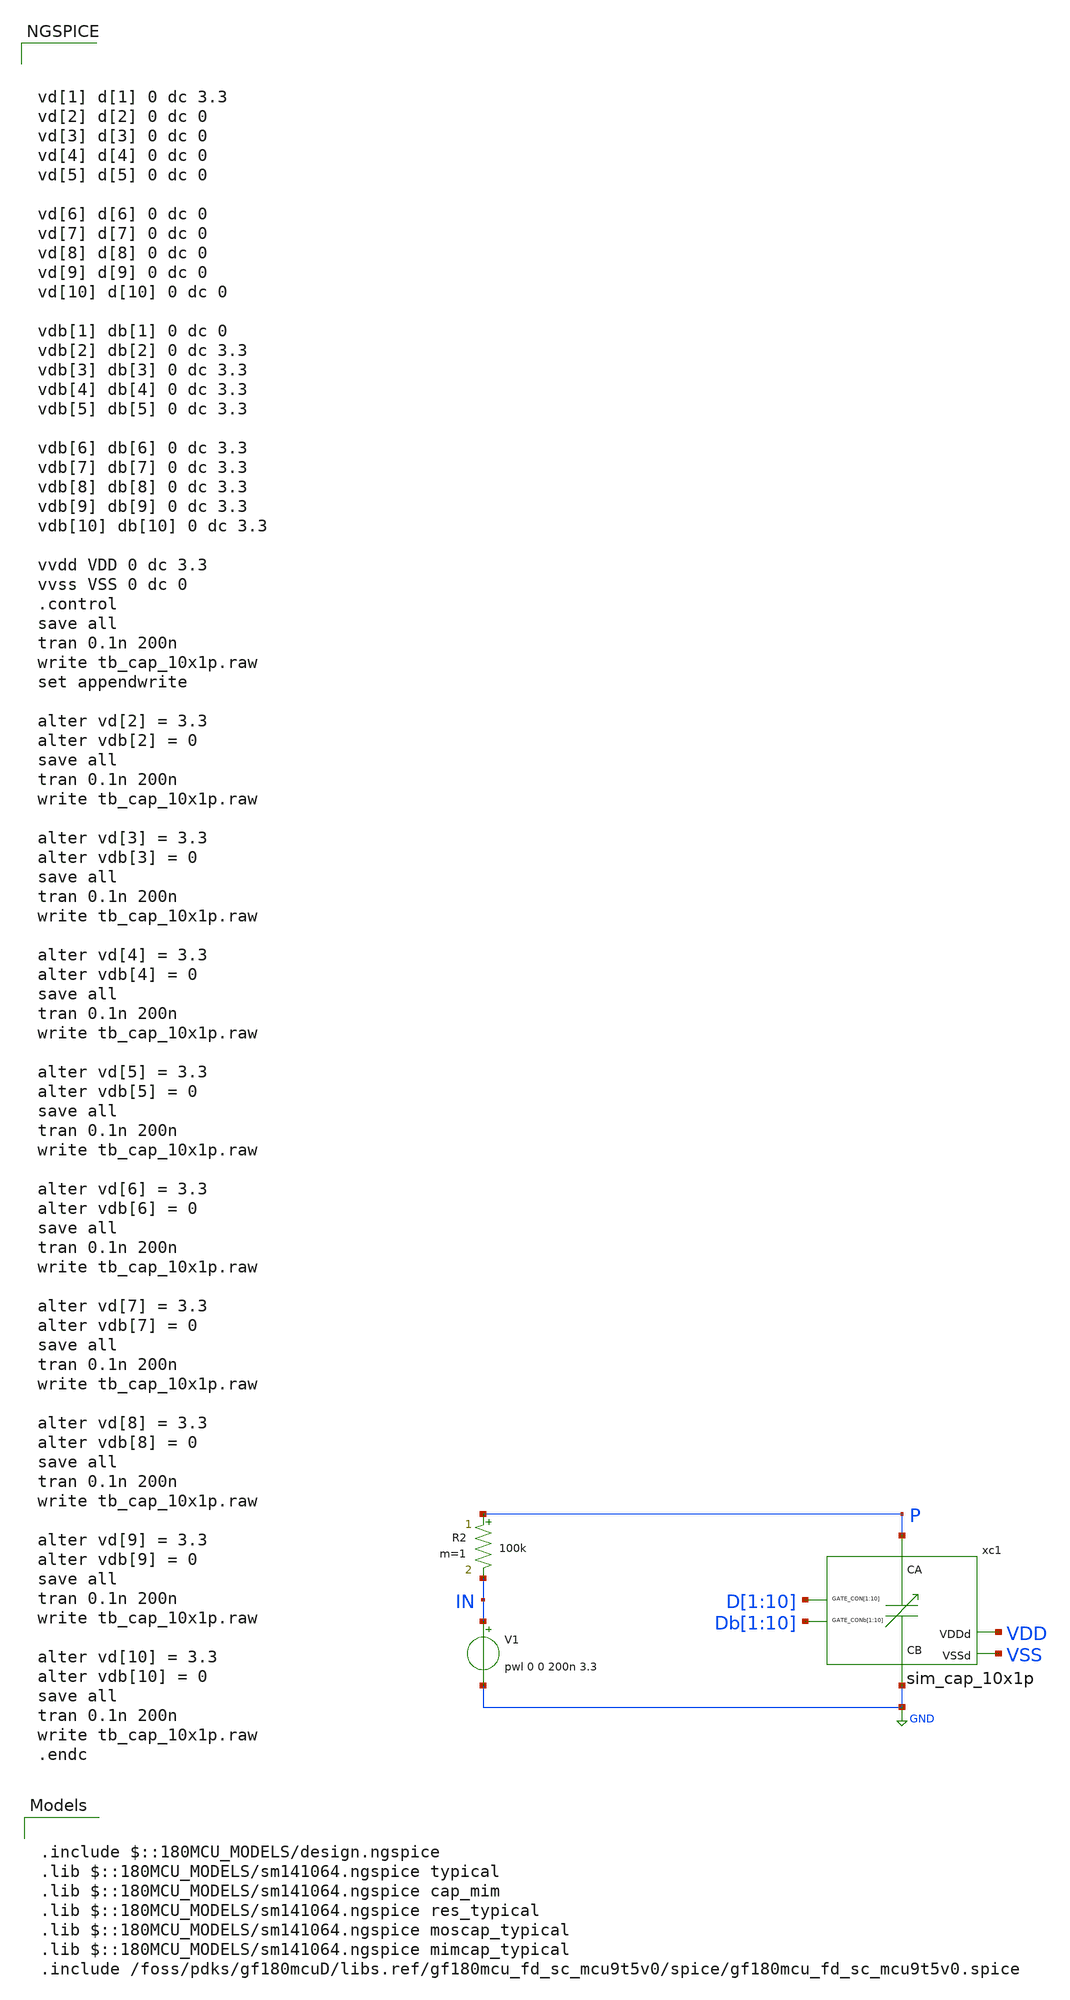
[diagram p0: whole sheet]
** sch_path: designs/libs/tb_passive_array/tb_cap_10x1p.sch
**.subckt tb_cap_10x1p
xc1 D[1] D[2] D[3] D[4] D[5] D[6] D[7] D[8] D[9] D[10] Db[1] Db[2] Db[3] Db[4] Db[5] Db[6] Db[7]
+ Db[8] Db[9] Db[10] VDD VSS P GND sim_cap_10x1p
V1 IN GND pwl 0 0 200n 3.3
R2 P IN 100k m=1
**** begin user architecture code

.include $::180MCU_MODELS/design.ngspice
.lib $::180MCU_MODELS/sm141064.ngspice typical
.lib $::180MCU_MODELS/sm141064.ngspice cap_mim
.lib $::180MCU_MODELS/sm141064.ngspice res_typical
.lib $::180MCU_MODELS/sm141064.ngspice moscap_typical
.lib $::180MCU_MODELS/sm141064.ngspice mimcap_typical
.include /foss/pdks/gf180mcuD/libs.ref/gf180mcu_fd_sc_mcu9t5v0/spice/gf180mcu_fd_sc_mcu9t5v0.spice




vd[1] d[1] 0 dc 3.3
vd[2] d[2] 0 dc 0
vd[3] d[3] 0 dc 0
vd[4] d[4] 0 dc 0
vd[5] d[5] 0 dc 0

vd[6] d[6] 0 dc 0
vd[7] d[7] 0 dc 0
vd[8] d[8] 0 dc 0
vd[9] d[9] 0 dc 0
vd[10] d[10] 0 dc 0

vdb[1] db[1] 0 dc 0
vdb[2] db[2] 0 dc 3.3
vdb[3] db[3] 0 dc 3.3
vdb[4] db[4] 0 dc 3.3
vdb[5] db[5] 0 dc 3.3

vdb[6] db[6] 0 dc 3.3
vdb[7] db[7] 0 dc 3.3
vdb[8] db[8] 0 dc 3.3
vdb[9] db[9] 0 dc 3.3
vdb[10] db[10] 0 dc 3.3

vvdd VDD 0 dc 3.3
vvss VSS 0 dc 0
.control
save all
tran 0.1n 200n
write tb_cap_10x1p.raw
set appendwrite

alter vd[2] = 3.3
alter vdb[2] = 0
save all
tran 0.1n 200n
write tb_cap_10x1p.raw

alter vd[3] = 3.3
alter vdb[3] = 0
save all
tran 0.1n 200n
write tb_cap_10x1p.raw

alter vd[4] = 3.3
alter vdb[4] = 0
save all
tran 0.1n 200n
write tb_cap_10x1p.raw

alter vd[5] = 3.3
alter vdb[5] = 0
save all
tran 0.1n 200n
write tb_cap_10x1p.raw

alter vd[6] = 3.3
alter vdb[6] = 0
save all
tran 0.1n 200n
write tb_cap_10x1p.raw

alter vd[7] = 3.3
alter vdb[7] = 0
save all
tran 0.1n 200n
write tb_cap_10x1p.raw

alter vd[8] = 3.3
alter vdb[8] = 0
save all
tran 0.1n 200n
write tb_cap_10x1p.raw

alter vd[9] = 3.3
alter vdb[9] = 0
save all
tran 0.1n 200n
write tb_cap_10x1p.raw

alter vd[10] = 3.3
alter vdb[10] = 0
save all
tran 0.1n 200n
write tb_cap_10x1p.raw
.endc


**** end user architecture code
**.ends
.GLOBAL GND
.end
